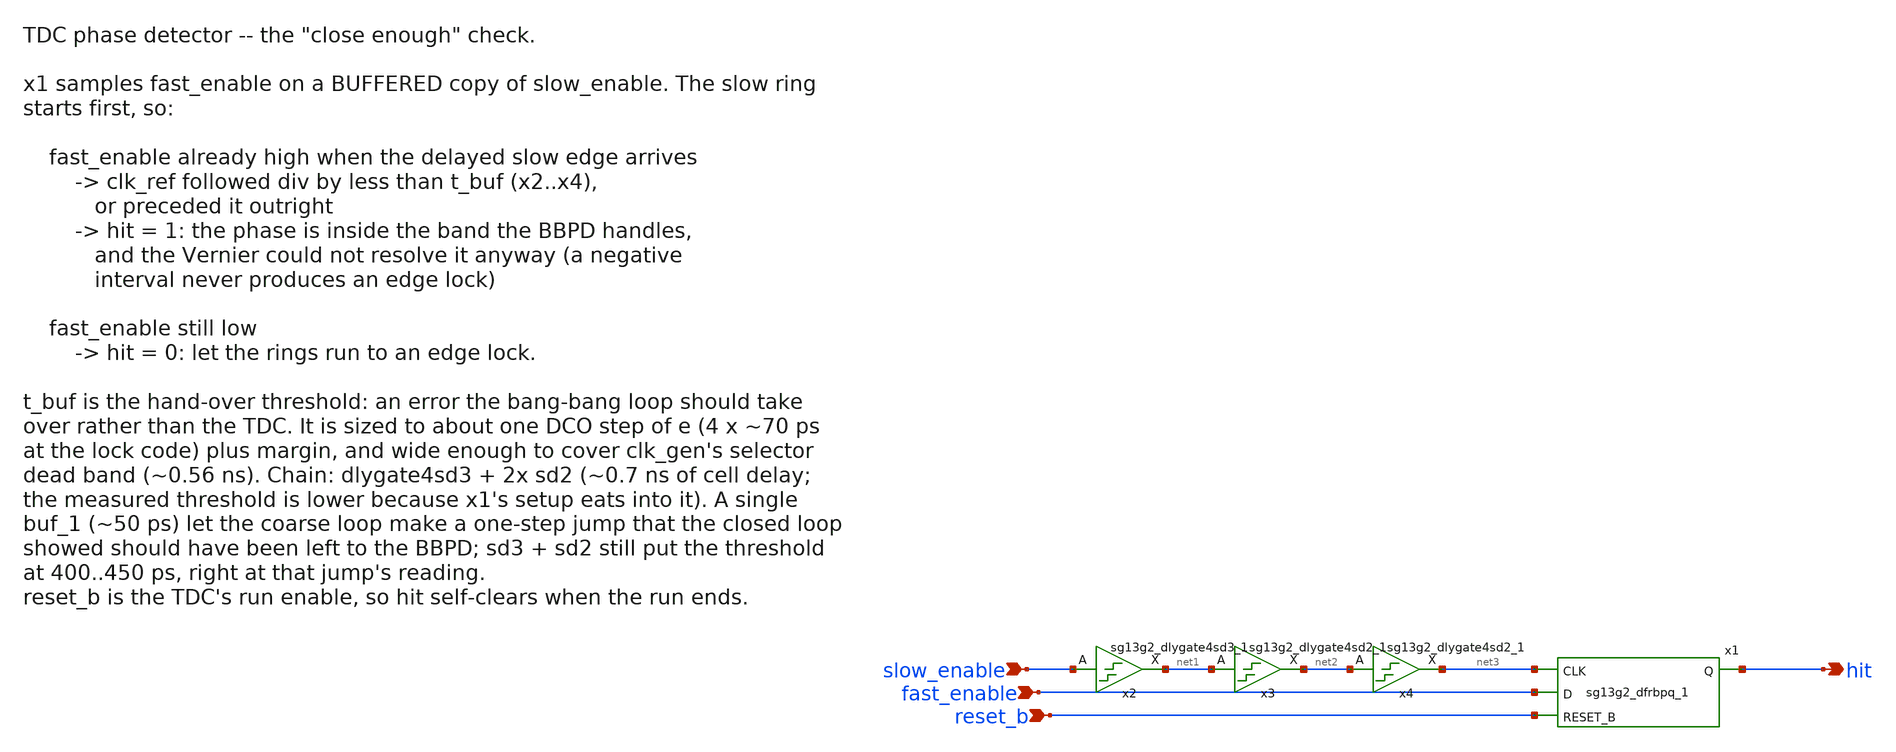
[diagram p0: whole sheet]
** sch_path: TPU5555-main/mdll/mixed_signal_design_blocks/tdc/src/tdc_pd.sch
* IHP-GmbH/IHP-Open-PDK/ihp-sg13g2/libs.tech/xschem/sg13g2_stdcells/sg13g2_dlygate4sd2_1.sch:
* Copyright 2023 IHP PDK Authors
* Licensed under the Apache License, Version 2.0 (the "License");
**.subckt tdc_pd slow_enable fast_enable reset_b hit
*.ipin slow_enable
*.ipin fast_enable
*.ipin reset_b
*.opin hit
x1 hit net3 fast_enable reset_b VDD VSS sg13g2_dfrbpq_1
x2 net1 slow_enable VDD VSS sg13g2_dlygate4sd3_1
x3 net2 net1 VDD VSS sg13g2_dlygate4sd2_1
x4 net3 net2 VDD VSS sg13g2_dlygate4sd2_1
**.ends

* expanding   symbol:  sg13g2_dfrbpq_1.sym # of pins=4
** sym_path: sg13g2_dfrbpq_1.sym
** sch_path: sg13g2_dfrbpq_1.sch
.subckt sg13g2_dfrbpq_1 Q CLK D RESET_B VDD VSS
*.opin Q
*.ipin CLK
*.ipin D
*.ipin RESET_B
*.iopin VDD
*.iopin VSS
XM1 Db D net10 VSS sg13_lv_nmos w=420.00n l=130.00n ng=1 m=1 mm_ok=1
XM2 net10 RESET_B VSS VSS sg13_lv_nmos w=420.00n l=130.00n ng=1 m=1 mm_ok=1
XM3 net1 clkneg net9 VSS sg13_lv_nmos w=420.00n l=130.00n ng=1 m=1 mm_ok=1
XM4 net9 net1 VSS VSS sg13_lv_nmos w=420.00n l=130.00n ng=1 m=1 mm_ok=1
XM5 net1 net1 net5 VSS sg13_lv_nmos w=420.00n l=130.00n ng=1 m=1 mm_ok=1
XM6 net5 RESET_B VSS VSS sg13_lv_nmos w=420.00n l=130.00n ng=1 m=1 mm_ok=1
XM7 net2 net1 VSS VSS sg13_lv_nmos w=740.00n l=130.00n ng=1 m=1 mm_ok=1
XM8 Q net2 VSS VSS sg13_lv_nmos w=740.00n l=130.00n ng=1 m=1 mm_ok=1
XM9 clkneg CLK VSS VSS sg13_lv_nmos w=740.00n l=130.00n ng=1 m=1 mm_ok=1
XM10 clkpos clkneg VSS VSS sg13_lv_nmos w=740.00n l=130.00n ng=1 m=1 mm_ok=1
XM11 Db clkneg net3 VSS sg13_lv_nmos w=420.00n l=130.00n ng=1 m=1 mm_ok=1
XM12 net3 clkpos net8 VSS sg13_lv_nmos w=420.00n l=130.00n ng=1 m=1 mm_ok=1
XM13 net8 net3 net4 VSS sg13_lv_nmos w=420.00n l=130.00n ng=1 m=1 mm_ok=1
XM14 net4 RESET_B VSS VSS sg13_lv_nmos w=420.00n l=130.00n ng=1 m=1 mm_ok=1
XM15 net3 net3 VSS VSS sg13_lv_nmos w=740.00n l=130.00n ng=1 m=1 mm_ok=1
XM16 net3 clkpos net1 VSS sg13_lv_nmos w=740.00n l=130.00n ng=1 m=1 mm_ok=1
XM17 Db RESET_B VDD VDD sg13_lv_pmos w=420.00n l=130.00n ng=1 m=1 mm_ok=1
XM18 Db D VDD VDD sg13_lv_pmos w=420.00n l=130.00n ng=1 m=1 mm_ok=1
XM19 net7 net1 VDD VDD sg13_lv_pmos w=420.00n l=130.00n ng=1 m=1 mm_ok=1
XM20 net1 clkpos net7 VDD sg13_lv_pmos w=420.00n l=130.00n ng=1 m=1 mm_ok=1
XM21 net1 net1 VDD VDD sg13_lv_pmos w=420.00n l=130.00n ng=1 m=1 mm_ok=1
XM22 net1 RESET_B VDD VDD sg13_lv_pmos w=420.00n l=130.00n ng=1 m=1 mm_ok=1
XM23 net2 net1 VDD VDD sg13_lv_pmos w=1.12u l=130.00n ng=1 m=1 mm_ok=1
XM24 Q net2 VDD VDD sg13_lv_pmos w=1.12u l=130.00n ng=1 m=1 mm_ok=1
XM25 clkneg CLK VDD VDD sg13_lv_pmos w=1.12u l=130.00n ng=1 m=1 mm_ok=1
XM26 clkpos clkneg VDD VDD sg13_lv_pmos w=1.12u l=130.00n ng=1 m=1 mm_ok=1
XM27 Db clkpos net3 VDD sg13_lv_pmos w=420.00n l=130.00n ng=1 m=1 mm_ok=1
XM28 net6 net3 VDD VDD sg13_lv_pmos w=420.00n l=130.00n ng=1 m=1 mm_ok=1
XM29 net3 clkneg net6 VDD sg13_lv_pmos w=420.00n l=130.00n ng=1 m=1 mm_ok=1
XM30 net3 RESET_B VDD VDD sg13_lv_pmos w=420.00n l=130.00n ng=1 m=1 mm_ok=1
XM31 net3 net3 VDD VDD sg13_lv_pmos w=1.000u l=130.00n ng=1 m=1 mm_ok=1
XM32 net3 clkneg net1 VDD sg13_lv_pmos w=1.000u l=130.00n ng=1 m=1 mm_ok=1
.ends


* expanding   symbol:  sg13g2_dlygate4sd3_1.sym # of pins=2
** sym_path: sg13g2_dlygate4sd3_1.sym
** sch_path: sg13g2_dlygate4sd3_1.sch
.subckt sg13g2_dlygate4sd3_1 X A VDD VSS
*.ipin A
*.opin X
*.iopin VDD
*.iopin VSS
XM1 net3 A VSS VSS sg13_lv_nmos w=420.00n l=130.00n ng=1 m=1 mm_ok=1
XM2 net1 net3 VSS VSS sg13_lv_nmos w=420.00n l=500.0n ng=1 m=1 mm_ok=1
XM3 net2 net1 VSS VSS sg13_lv_nmos w=420.00n l=500.0n ng=1 m=1 mm_ok=1
XM4 X net2 VSS VSS sg13_lv_nmos w=740.00n l=130.00n ng=1 m=1 mm_ok=1
XM5 net3 A VDD VDD sg13_lv_pmos w=420.00n l=130.00n ng=1 m=1 mm_ok=1
XM6 net1 net3 VDD VDD sg13_lv_pmos w=1.000u l=500.0n ng=1 m=1 mm_ok=1
XM7 net2 net1 VDD VDD sg13_lv_pmos w=1.000u l=500.0n ng=1 m=1 mm_ok=1
XM8 X net2 VDD VDD sg13_lv_pmos w=1.12u l=130.00n ng=1 m=1 mm_ok=1
.ends


* expanding   symbol:  sg13g2_dlygate4sd2_1.sym # of pins=2
** sym_path: sg13g2_dlygate4sd2_1.sym
** sch_path: sg13g2_dlygate4sd2_1.sch
.subckt sg13g2_dlygate4sd2_1 X A VDD VSS
*.ipin A
*.opin X
*.iopin VDD
*.iopin VSS
XM1 net2 A VSS VSS sg13_lv_nmos w=420.00n l=130.00n ng=1 m=1 mm_ok=1
XM2 net1 net2 VSS VSS sg13_lv_nmos w=420.00n l=180.00n ng=1 m=1 mm_ok=1
XM3 net3 net1 VSS VSS sg13_lv_nmos w=420.00n l=180.00n ng=1 m=1 mm_ok=1
XM4 X net3 VSS VSS sg13_lv_nmos w=740.00n l=130.00n ng=1 m=1 mm_ok=1
XM5 net2 A VDD VDD sg13_lv_pmos w=420.00n l=130.00n ng=1 m=1 mm_ok=1
XM6 net1 net2 VDD VDD sg13_lv_pmos w=1.000u l=250.00n ng=1 m=1 mm_ok=1
XM7 net3 net1 VDD VDD sg13_lv_pmos w=1.000u l=250.00n ng=1 m=1 mm_ok=1
XM8 X net3 VDD VDD sg13_lv_pmos w=1.12u l=130.00n ng=1 m=1 mm_ok=1
.ends

.end
